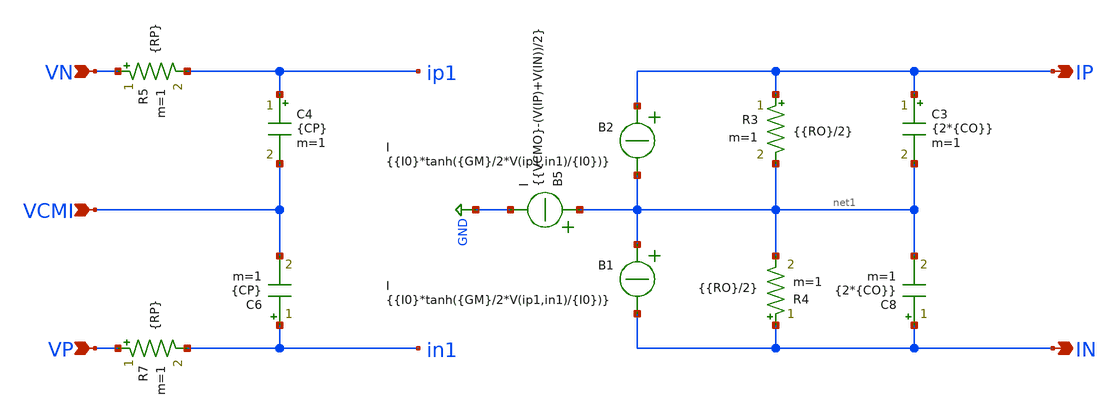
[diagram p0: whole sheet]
** sch_path: circuit-level/xschem/macro-models/ota_fd_2pole.sch
**.subckt ota_fd_2pole VP VN IP IN VCMI
*.ipin VP
*.ipin VN
*.opin IP
*.opin IN
*.ipin VCMI
R3 IP net1 {{RO}/2} m=1
R4 IN net1 {{RO}/2} m=1
C3 IP net1 {2*{CO}} m=1
R5 VN ip1 {RP} m=1
C4 ip1 VCMI {CP} m=1
C6 in1 VCMI {CP} m=1
C8 IN net1 {2*{CO}} m=1
R7 VP in1 {RP} m=1
B2 IP net1 I = {{I0}*tanh({GM}/2*V(ip1,in1)/{I0})}
B1 net1 IN I = {{I0}*tanh({GM}/2*V(ip1,in1)/{I0})}
B5 net1 GND I = {{VCMO}-(V(IP)+V(IN))/2}
**.ends
.GLOBAL GND
.end
